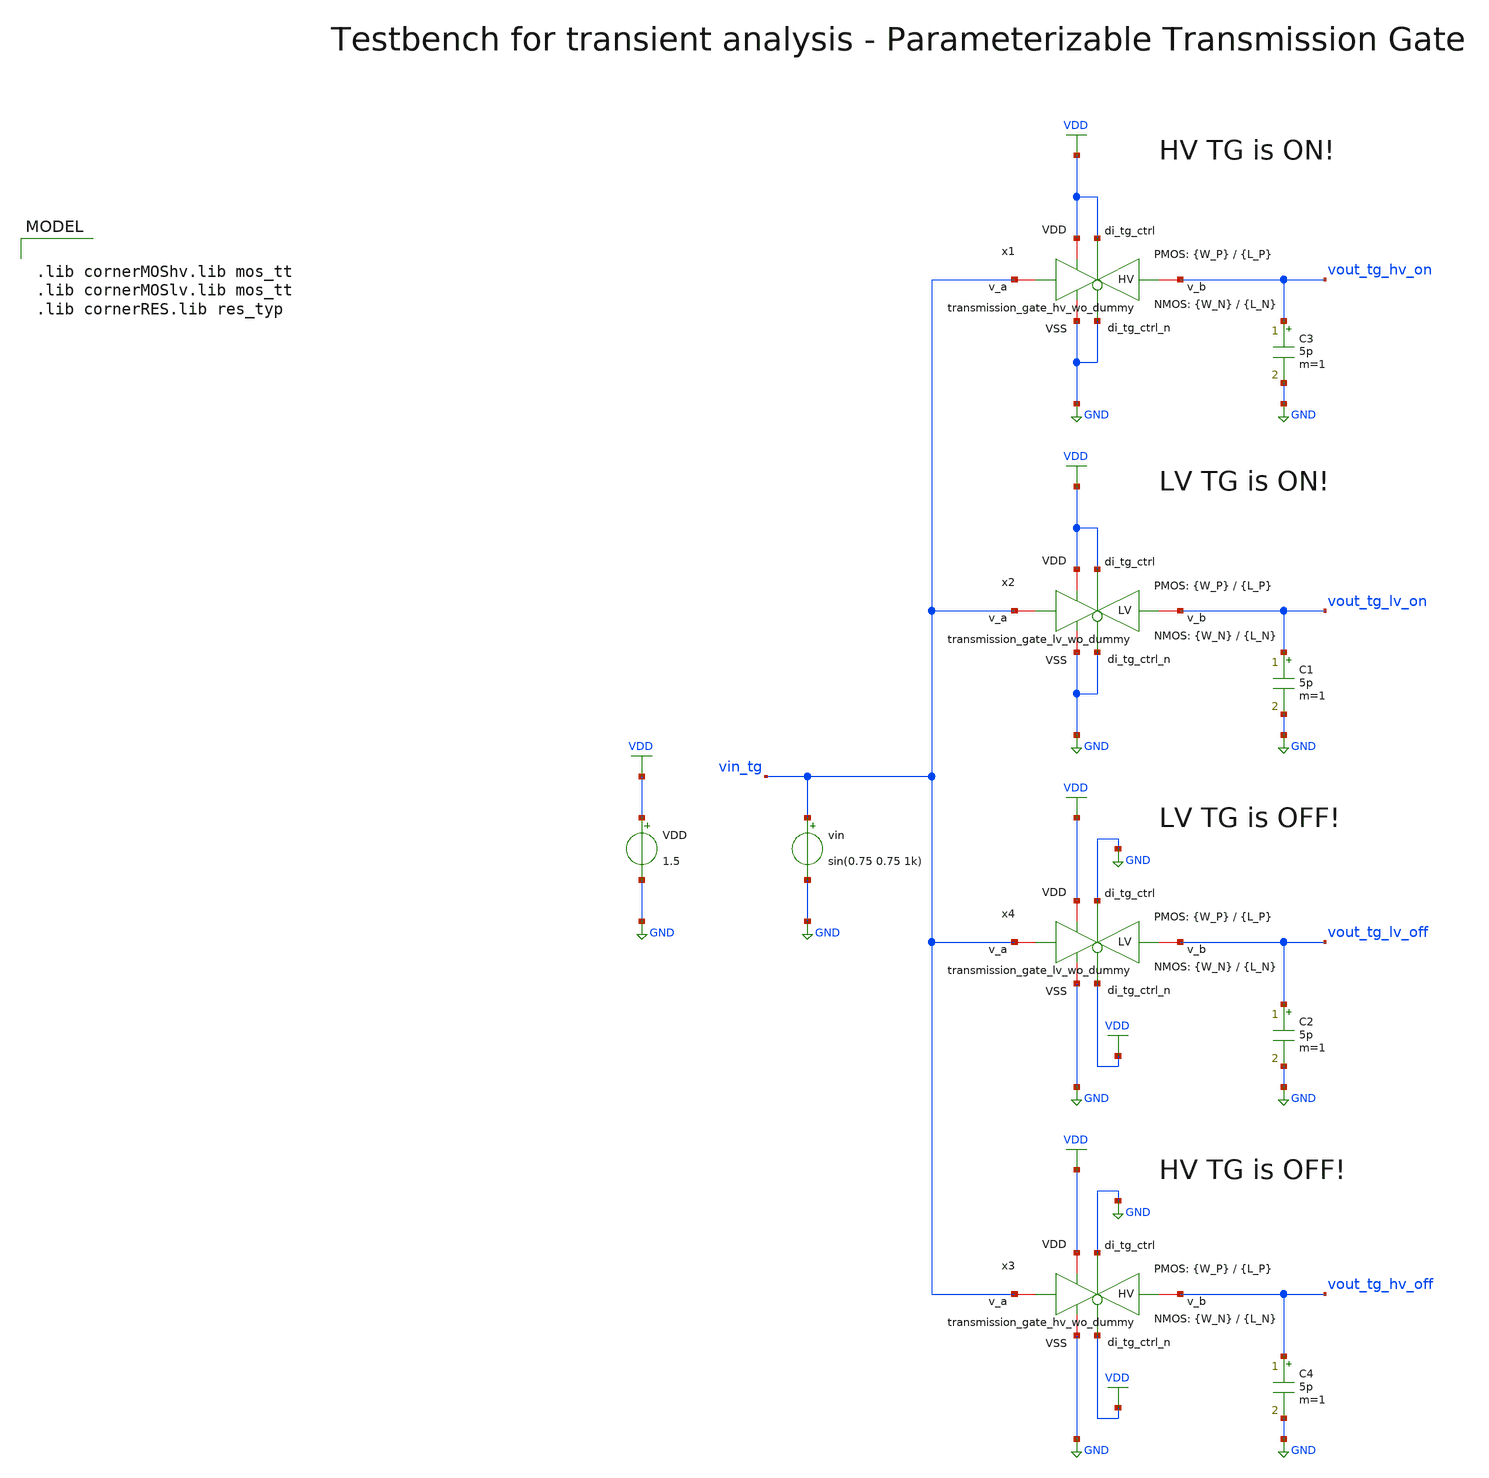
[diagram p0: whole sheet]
** sch_path: SG13G2_ATBS-ADC-main/xschem/transmission_gate/testbenches/transmission_gate_tb_tran.sch
**.subckt transmission_gate_tb_tran
VDD VDD GND 1.5
vin vin_tg GND sin(0.75 0.75 1k)
C1 vout_tg_lv_on GND 5p m=1
C2 vout_tg_lv_off GND 5p m=1
C3 vout_tg_hv_on GND 5p m=1
C4 vout_tg_hv_off GND 5p m=1
x1 VDD VDD GND vout_tg_hv_on vin_tg GND transmission_gate_hv_wo_dummy W_P={W_P} L_P={L_P} W_N={W_N} L_N={L_N}
x2 VDD VDD GND vout_tg_lv_on vin_tg GND transmission_gate_lv_wo_dummy W_P={W_P} L_P={L_P} W_N={W_N} L_N={L_N}
x3 VDD GND GND vout_tg_hv_off vin_tg VDD transmission_gate_hv_wo_dummy W_P={W_P} L_P={L_P} W_N={W_N}
+ L_N={L_N}
x4 VDD GND GND vout_tg_lv_off vin_tg VDD transmission_gate_lv_wo_dummy W_P={W_P} L_P={L_P} W_N={W_N}
+ L_N={L_N}
**** begin user architecture code

.lib cornerMOShv.lib mos_tt
.lib cornerMOSlv.lib mos_tt
.lib cornerRES.lib res_typ



.param temp=27
.param W_N=1u
.param L_N=0.5u
.param W_P=1u
.param L_P=0.5u
.options savecurrents
.control

save all

* Operating Point Analysis
op
remzerovec
write transmission_gate_tb_tran.raw
set appendwrite

* Transient Analysis
tran 10u 4ms
write transmission_gate_tb_tran.raw

plot vin_tg vout_tg_lv_on vout_tg_hv_on
plot vin_tg vout_tg_lv_off vout_tg_hv_off

* Writing Data
set wr_singlescale
set wr_vecnames
wrdata /foss/designs/SG13G2_ATBS-ADC-main/python/plot_simulations/data/transmission_gate_tb_tran.txt
+ v(vin_tg) v(vout_tg_lv_on) v(vout_tg_hv_on) v(vout_tg_lv_off) v(vout_tg_hv_off)


*quit
.endc

**** end user architecture code
**.ends

* expanding   symbol:  transmission_gate/transmission_gate_hv_wo_dummy.sym # of pins=6
** sym_path: SG13G2_ATBS-ADC-main/xschem/transmission_gate/transmission_gate_hv_wo_dummy.sym
** sch_path: SG13G2_ATBS-ADC-main/xschem/transmission_gate/transmission_gate_hv_wo_dummy.sch
.subckt transmission_gate_hv_wo_dummy VDD di_tg_ctrl VSS v_b v_a di_tg_ctrl_n  W_P=1.0u L_P=0.5u
+ W_N=1.0u L_N=0.5u
*.iopin v_a
*.iopin v_b
*.iopin VDD
*.iopin VSS
*.ipin di_tg_ctrl
*.ipin di_tg_ctrl_n
XM1 v_a di_tg_ctrl v_b VSS sg13_hv_nmos w=W_N l=L_N ng=1 m=1 mm_ok=1
XM2 v_a di_tg_ctrl_n v_b VDD sg13_hv_pmos w=W_P l=L_P ng=1 m=1 mm_ok=1
.ends


* expanding   symbol:  transmission_gate/transmission_gate_lv_wo_dummy.sym # of pins=6
** sym_path: SG13G2_ATBS-ADC-main/xschem/transmission_gate/transmission_gate_lv_wo_dummy.sym
** sch_path: SG13G2_ATBS-ADC-main/xschem/transmission_gate/transmission_gate_lv_wo_dummy.sch
.subckt transmission_gate_lv_wo_dummy VDD di_tg_ctrl VSS v_b v_a di_tg_ctrl_n  W_P=1.0u L_P=0.13u
+ W_N=1.0u L_N=0.13u
*.iopin v_a
*.iopin v_b
*.iopin VDD
*.iopin VSS
*.ipin di_tg_ctrl
*.ipin di_tg_ctrl_n
XM1 v_a di_tg_ctrl v_b VSS sg13_lv_nmos w=W_N l=L_N ng=1 m=1 mm_ok=1
XM2 v_a di_tg_ctrl_n v_b VDD sg13_lv_pmos w=W_P l=L_P ng=1 m=1 mm_ok=1
.ends

.GLOBAL GND
.GLOBAL VDD
.end
